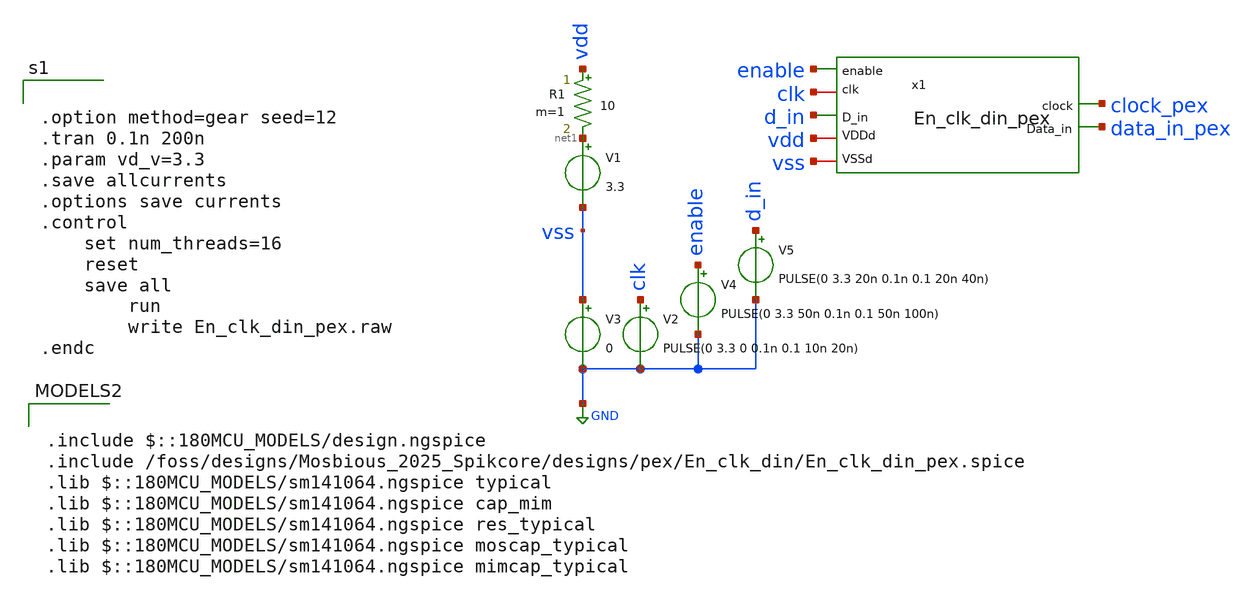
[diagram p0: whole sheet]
** sch_path: designs/pex/En_clk_din/En_clk_din_pex.sch
**.subckt En_clk_din_pex
V1 net1 vss 3.3
R1 vdd net1 10 m=1
V3 vss GND 0
x1 vdd vss clk clock_pex enable d_in data_in_pex En_clk_din_pex
V2 clk GND PULSE(0 3.3 0 0.1n 0.1 10n 20n)
V4 enable GND PULSE(0 3.3 50n 0.1n 0.1 50n 100n)
V5 d_in GND PULSE(0 3.3 20n 0.1n 0.1 20n 40n)
**** begin user architecture code


.option method=gear seed=12
.tran 0.1n 200n
.param vd_v=3.3
.save allcurrents
.options save currents
.control
	set num_threads=16
	reset
	save all
        run
        write En_clk_din_pex.raw
.endc



.include $::180MCU_MODELS/design.ngspice
.include /foss/designs/Mosbious_2025_Spikcore/designs/pex/En_clk_din/En_clk_din_pex.spice
.lib $::180MCU_MODELS/sm141064.ngspice typical
.lib $::180MCU_MODELS/sm141064.ngspice cap_mim
.lib $::180MCU_MODELS/sm141064.ngspice res_typical
.lib $::180MCU_MODELS/sm141064.ngspice moscap_typical
.lib $::180MCU_MODELS/sm141064.ngspice mimcap_typical

**** end user architecture code
**.ends
.GLOBAL GND
.end
